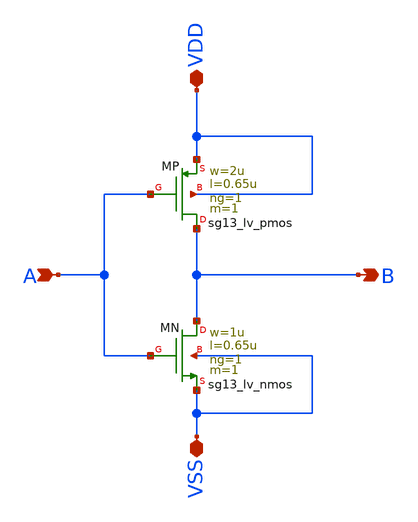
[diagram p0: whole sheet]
** sch_path: OSC9996-main/schematic/xschem/gate_inv_L0d65.sch
**.subckt gate_inv_L0d65 B A VDD VSS
*.opin B
*.ipin A
*.iopin VDD
*.iopin VSS
XMN B A VSS VSS sg13_lv_nmos w=1u l=0.65u ng=1 m=1 mm_ok=1
XMP B A VDD VDD sg13_lv_pmos w=2u l=0.65u ng=1 m=1 mm_ok=1
**.ends
.end
